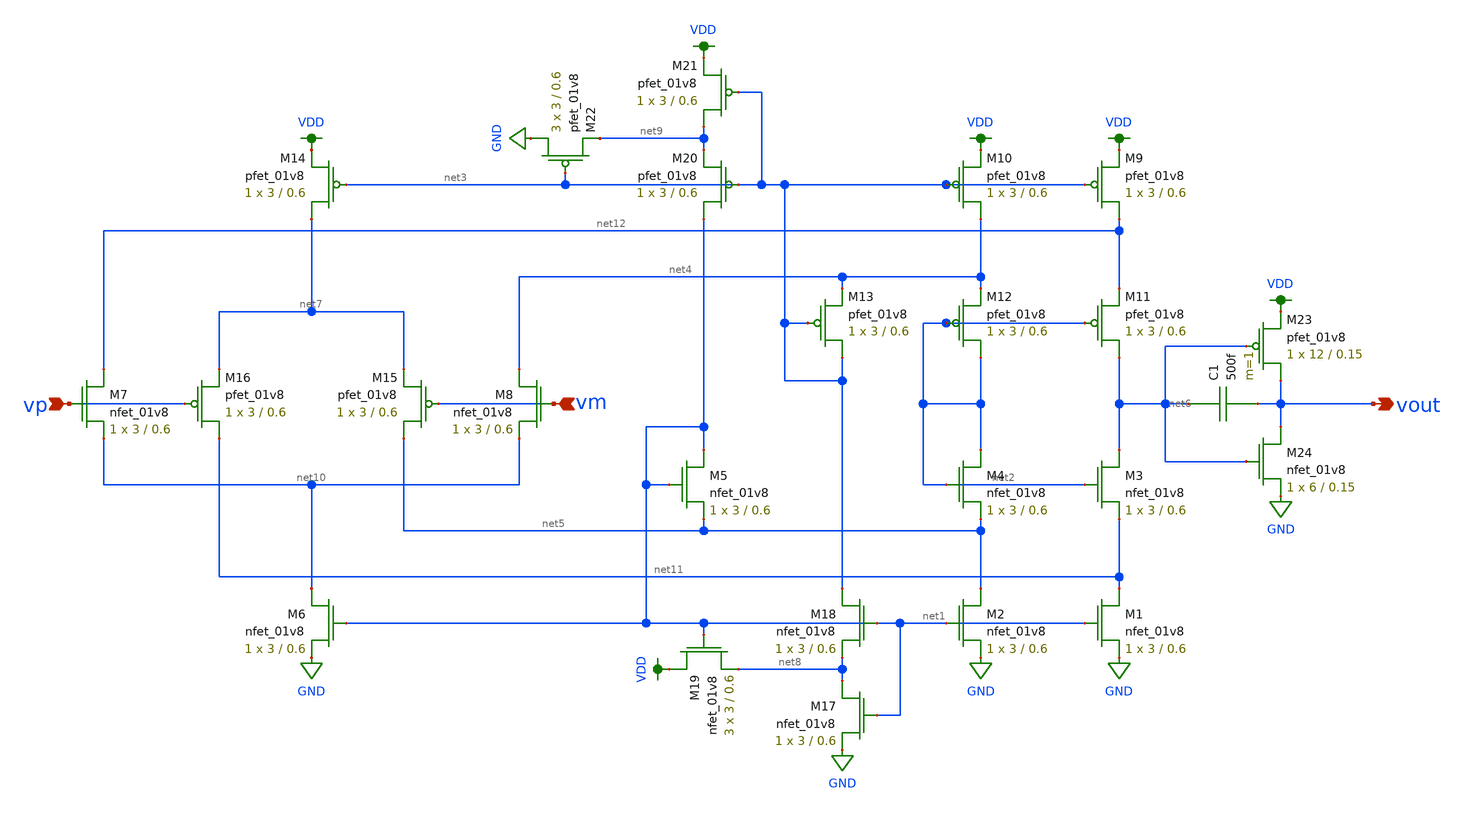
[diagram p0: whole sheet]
** sch_path: Final DAC files/schematics/opamp/selfbiasedcascode2stage.sch
**.subckt selfbiasedcascode2stage vp vm vout
*.ipin vp
*.ipin vm
*.opin vout
XM1 net11 net1 GND GND sky130_fd_pr__nfet_01v8 L=0.6 W=3 nf=1 ad='int((nf+1)/2) * W/nf * 0.29' as='int((nf+2)/2) * W/nf * 0.29'
+ pd='2*int((nf+1)/2) * (W/nf + 0.29)' ps='2*int((nf+2)/2) * (W/nf + 0.29)' nrd='0.29 / W' nrs='0.29 / W'
+ sa=0 sb=0 sd=0 mult=1 m=1
XM9 net12 net3 VDD VDD sky130_fd_pr__pfet_01v8 L=0.6 W=3 nf=1 ad='int((nf+1)/2) * W/nf * 0.29' as='int((nf+2)/2) * W/nf * 0.29'
+ pd='2*int((nf+1)/2) * (W/nf + 0.29)' ps='2*int((nf+2)/2) * (W/nf + 0.29)' nrd='0.29 / W' nrs='0.29 / W'
+ sa=0 sb=0 sd=0 mult=1 m=1
XM2 net5 net1 GND GND sky130_fd_pr__nfet_01v8 L=0.6 W=3 nf=1 ad='int((nf+1)/2) * W/nf * 0.29' as='int((nf+2)/2) * W/nf * 0.29'
+ pd='2*int((nf+1)/2) * (W/nf + 0.29)' ps='2*int((nf+2)/2) * (W/nf + 0.29)' nrd='0.29 / W' nrs='0.29 / W'
+ sa=0 sb=0 sd=0 mult=1 m=1
XM3 net6 net2 net11 GND sky130_fd_pr__nfet_01v8 L=0.6 W=3 nf=1 ad='int((nf+1)/2) * W/nf * 0.29' as='int((nf+2)/2) * W/nf * 0.29'
+ pd='2*int((nf+1)/2) * (W/nf + 0.29)' ps='2*int((nf+2)/2) * (W/nf + 0.29)' nrd='0.29 / W' nrs='0.29 / W'
+ sa=0 sb=0 sd=0 mult=1 m=1
XM4 net2 net2 net5 GND sky130_fd_pr__nfet_01v8 L=0.6 W=3 nf=1 ad='int((nf+1)/2) * W/nf * 0.29' as='int((nf+2)/2) * W/nf * 0.29'
+ pd='2*int((nf+1)/2) * (W/nf + 0.29)' ps='2*int((nf+2)/2) * (W/nf + 0.29)' nrd='0.29 / W' nrs='0.29 / W'
+ sa=0 sb=0 sd=0 mult=1 m=1
XM5 net1 net1 net5 GND sky130_fd_pr__nfet_01v8 L=0.6 W=3 nf=1 ad='int((nf+1)/2) * W/nf * 0.29' as='int((nf+2)/2) * W/nf * 0.29'
+ pd='2*int((nf+1)/2) * (W/nf + 0.29)' ps='2*int((nf+2)/2) * (W/nf + 0.29)' nrd='0.29 / W' nrs='0.29 / W'
+ sa=0 sb=0 sd=0 mult=1 m=1
XM6 net10 net1 GND GND sky130_fd_pr__nfet_01v8 L=0.6 W=3 nf=1 ad='int((nf+1)/2) * W/nf * 0.29' as='int((nf+2)/2) * W/nf * 0.29'
+ pd='2*int((nf+1)/2) * (W/nf + 0.29)' ps='2*int((nf+2)/2) * (W/nf + 0.29)' nrd='0.29 / W' nrs='0.29 / W'
+ sa=0 sb=0 sd=0 mult=1 m=1
XM7 net12 vp net10 GND sky130_fd_pr__nfet_01v8 L=0.6 W=3 nf=1 ad='int((nf+1)/2) * W/nf * 0.29' as='int((nf+2)/2) * W/nf * 0.29'
+ pd='2*int((nf+1)/2) * (W/nf + 0.29)' ps='2*int((nf+2)/2) * (W/nf + 0.29)' nrd='0.29 / W' nrs='0.29 / W'
+ sa=0 sb=0 sd=0 mult=1 m=1
XM8 net4 vm net10 GND sky130_fd_pr__nfet_01v8 L=0.6 W=3 nf=1 ad='int((nf+1)/2) * W/nf * 0.29' as='int((nf+2)/2) * W/nf * 0.29'
+ pd='2*int((nf+1)/2) * (W/nf + 0.29)' ps='2*int((nf+2)/2) * (W/nf + 0.29)' nrd='0.29 / W' nrs='0.29 / W'
+ sa=0 sb=0 sd=0 mult=1 m=1
XM10 net4 net3 VDD VDD sky130_fd_pr__pfet_01v8 L=0.6 W=3 nf=1 ad='int((nf+1)/2) * W/nf * 0.29' as='int((nf+2)/2) * W/nf * 0.29'
+ pd='2*int((nf+1)/2) * (W/nf + 0.29)' ps='2*int((nf+2)/2) * (W/nf + 0.29)' nrd='0.29 / W' nrs='0.29 / W'
+ sa=0 sb=0 sd=0 mult=1 m=1
XM11 net6 net2 net12 VDD sky130_fd_pr__pfet_01v8 L=0.6 W=3 nf=1 ad='int((nf+1)/2) * W/nf * 0.29' as='int((nf+2)/2) * W/nf * 0.29'
+ pd='2*int((nf+1)/2) * (W/nf + 0.29)' ps='2*int((nf+2)/2) * (W/nf + 0.29)' nrd='0.29 / W' nrs='0.29 / W'
+ sa=0 sb=0 sd=0 mult=1 m=1
XM12 net2 net2 net4 VDD sky130_fd_pr__pfet_01v8 L=0.6 W=3 nf=1 ad='int((nf+1)/2) * W/nf * 0.29' as='int((nf+2)/2) * W/nf * 0.29'
+ pd='2*int((nf+1)/2) * (W/nf + 0.29)' ps='2*int((nf+2)/2) * (W/nf + 0.29)' nrd='0.29 / W' nrs='0.29 / W'
+ sa=0 sb=0 sd=0 mult=1 m=1
XM13 net3 net3 net4 VDD sky130_fd_pr__pfet_01v8 L=0.6 W=3 nf=1 ad='int((nf+1)/2) * W/nf * 0.29' as='int((nf+2)/2) * W/nf * 0.29'
+ pd='2*int((nf+1)/2) * (W/nf + 0.29)' ps='2*int((nf+2)/2) * (W/nf + 0.29)' nrd='0.29 / W' nrs='0.29 / W'
+ sa=0 sb=0 sd=0 mult=1 m=1
XM14 net7 net3 VDD VDD sky130_fd_pr__pfet_01v8 L=0.6 W=3 nf=1 ad='int((nf+1)/2) * W/nf * 0.29' as='int((nf+2)/2) * W/nf * 0.29'
+ pd='2*int((nf+1)/2) * (W/nf + 0.29)' ps='2*int((nf+2)/2) * (W/nf + 0.29)' nrd='0.29 / W' nrs='0.29 / W'
+ sa=0 sb=0 sd=0 mult=1 m=1
XM15 net5 vm net7 VDD sky130_fd_pr__pfet_01v8 L=0.6 W=3 nf=1 ad='int((nf+1)/2) * W/nf * 0.29' as='int((nf+2)/2) * W/nf * 0.29'
+ pd='2*int((nf+1)/2) * (W/nf + 0.29)' ps='2*int((nf+2)/2) * (W/nf + 0.29)' nrd='0.29 / W' nrs='0.29 / W'
+ sa=0 sb=0 sd=0 mult=1 m=1
XM16 net11 vp net7 VDD sky130_fd_pr__pfet_01v8 L=0.6 W=3 nf=1 ad='int((nf+1)/2) * W/nf * 0.29' as='int((nf+2)/2) * W/nf * 0.29'
+ pd='2*int((nf+1)/2) * (W/nf + 0.29)' ps='2*int((nf+2)/2) * (W/nf + 0.29)' nrd='0.29 / W' nrs='0.29 / W'
+ sa=0 sb=0 sd=0 mult=1 m=1
XM17 net8 net1 GND GND sky130_fd_pr__nfet_01v8 L=0.6 W=3 nf=1 ad='int((nf+1)/2) * W/nf * 0.29' as='int((nf+2)/2) * W/nf * 0.29'
+ pd='2*int((nf+1)/2) * (W/nf + 0.29)' ps='2*int((nf+2)/2) * (W/nf + 0.29)' nrd='0.29 / W' nrs='0.29 / W'
+ sa=0 sb=0 sd=0 mult=1 m=1
XM18 net3 net1 net8 GND sky130_fd_pr__nfet_01v8 L=0.6 W=3 nf=1 ad='int((nf+1)/2) * W/nf * 0.29' as='int((nf+2)/2) * W/nf * 0.29'
+ pd='2*int((nf+1)/2) * (W/nf + 0.29)' ps='2*int((nf+2)/2) * (W/nf + 0.29)' nrd='0.29 / W' nrs='0.29 / W'
+ sa=0 sb=0 sd=0 mult=1 m=1
XM19 VDD net1 net8 GND sky130_fd_pr__nfet_01v8 L=0.6 W=3 nf=1 ad='int((nf+1)/2) * W/nf * 0.29' as='int((nf+2)/2) * W/nf * 0.29'
+ pd='2*int((nf+1)/2) * (W/nf + 0.29)' ps='2*int((nf+2)/2) * (W/nf + 0.29)' nrd='0.29 / W' nrs='0.29 / W'
+ sa=0 sb=0 sd=0 mult=3 m=3
XM20 net1 net3 net9 VDD sky130_fd_pr__pfet_01v8 L=0.6 W=3 nf=1 ad='int((nf+1)/2) * W/nf * 0.29' as='int((nf+2)/2) * W/nf * 0.29'
+ pd='2*int((nf+1)/2) * (W/nf + 0.29)' ps='2*int((nf+2)/2) * (W/nf + 0.29)' nrd='0.29 / W' nrs='0.29 / W'
+ sa=0 sb=0 sd=0 mult=1 m=1
XM21 net9 net3 VDD VDD sky130_fd_pr__pfet_01v8 L=0.6 W=3 nf=1 ad='int((nf+1)/2) * W/nf * 0.29' as='int((nf+2)/2) * W/nf * 0.29'
+ pd='2*int((nf+1)/2) * (W/nf + 0.29)' ps='2*int((nf+2)/2) * (W/nf + 0.29)' nrd='0.29 / W' nrs='0.29 / W'
+ sa=0 sb=0 sd=0 mult=1 m=1
XM22 GND net3 net9 VDD sky130_fd_pr__pfet_01v8 L=0.6 W=3 nf=1 ad='int((nf+1)/2) * W/nf * 0.29' as='int((nf+2)/2) * W/nf * 0.29'
+ pd='2*int((nf+1)/2) * (W/nf + 0.29)' ps='2*int((nf+2)/2) * (W/nf + 0.29)' nrd='0.29 / W' nrs='0.29 / W'
+ sa=0 sb=0 sd=0 mult=3 m=3
XM23 vout net6 VDD VDD sky130_fd_pr__pfet_01v8 L=0.15 W=12 nf=1 ad='int((nf+1)/2) * W/nf * 0.29' as='int((nf+2)/2) * W/nf * 0.29'
+ pd='2*int((nf+1)/2) * (W/nf + 0.29)' ps='2*int((nf+2)/2) * (W/nf + 0.29)' nrd='0.29 / W' nrs='0.29 / W'
+ sa=0 sb=0 sd=0 mult=1 m=1
XM24 vout net6 GND GND sky130_fd_pr__nfet_01v8 L=0.15 W=6 nf=1 ad='int((nf+1)/2) * W/nf * 0.29' as='int((nf+2)/2) * W/nf * 0.29'
+ pd='2*int((nf+1)/2) * (W/nf + 0.29)' ps='2*int((nf+2)/2) * (W/nf + 0.29)' nrd='0.29 / W' nrs='0.29 / W'
+ sa=0 sb=0 sd=0 mult=1 m=1
C1 net6 vout 500f m=1
**.ends
.GLOBAL GND
.GLOBAL VDD
.end
